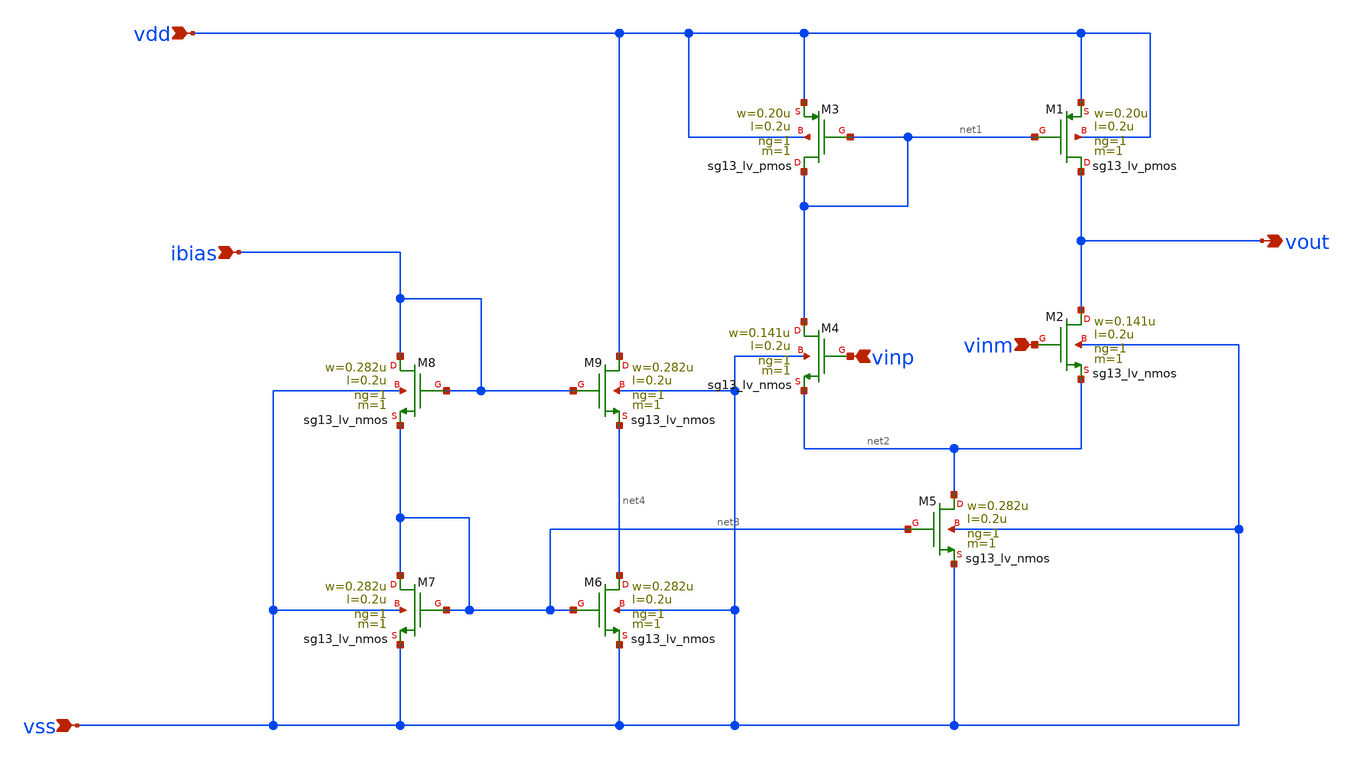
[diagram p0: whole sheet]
** sch_path: design/basic_5t_-ota.sch
**.subckt basic_5t_-ota vss vdd ibias vinm vinp vout
*.ipin vss
*.ipin vdd
*.ipin ibias
*.ipin vinm
*.ipin vinp
*.opin vout
XM1 vout net1 vdd vdd sg13_lv_pmos w=0.20u l=0.2u ng=1 m=1 mm_ok=1
XM2 vout vinm net2 vss sg13_lv_nmos w=0.141u l=0.2u ng=1 m=1 mm_ok=1
XM3 net1 net1 vdd vdd sg13_lv_pmos w=0.20u l=0.2u ng=1 m=1 mm_ok=1
XM4 net1 vinp net2 vss sg13_lv_nmos w=0.141u l=0.2u ng=1 m=1 mm_ok=1
XM5 net2 net3 vss vss sg13_lv_nmos w=0.282u l=0.2u ng=1 m=1 mm_ok=1
XM6 net4 net3 vss vss sg13_lv_nmos w=0.282u l=0.2u ng=1 m=1 mm_ok=1
XM7 net3 net3 vss vss sg13_lv_nmos w=0.282u l=0.2u ng=1 m=1 mm_ok=1
XM9 vdd ibias net4 vss sg13_lv_nmos w=0.282u l=0.2u ng=1 m=1 mm_ok=1
XM8 ibias ibias net3 vss sg13_lv_nmos w=0.282u l=0.2u ng=1 m=1 mm_ok=1
**.ends
.end
